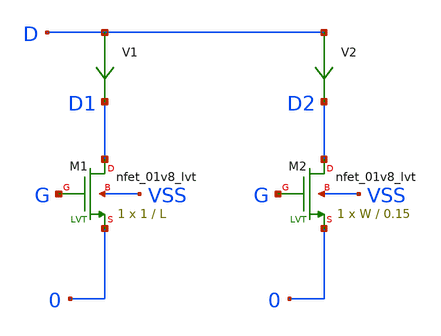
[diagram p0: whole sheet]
** sch_path: sky130_tests/test_nmos_sizes.sch
* Copyright 2021 Stefan Frederik Schippers
* Licensed under the Apache License, Version 2.0 (the "License");
* you may not use this file except in compliance with the License.
* You may obtain a copy of the License at
* https://www.apache.org/licenses/LICENSE-2.0
* Unless required by applicable law or agreed to in writing, software
* distributed under the License is distributed on an "AS IS" BASIS,
* WITHOUT WARRANTIES OR CONDITIONS OF ANY KIND, either express or implied.
* See the License for the specific language governing permissions and
* limitations under the License.
**.subckt test_nmos_sizes
XM1 D1 G 0 VSS sky130_fd_pr__nfet_01v8_lvt L=L W=1 nf=1 ad='W * 0.29' as='W * 0.29' pd='2 * (W + 0.29)'
+ ps='2 * (W + 0.29)' nrd='0.29 / W' nrs='0.29 / W' sa=0 sb=0 sd=0 mult=1 m=1
XM2 D2 G 0 VSS sky130_fd_pr__nfet_01v8_lvt L=0.15 W=W nf=1 ad='W * 0.29' as='W * 0.29' pd='2 * (W + 0.29)'
+ ps='2 * (W + 0.29)' nrd='0.29 / W' nrs='0.29 / W' sa=0 sb=0 sd=0 mult=1 m=1
V2 D D2 0
.save i(v2)
V1 D D1 0
.save i(v1)
**** begin user architecture code
 ** manual skywater pdks install (with patches applied)
* .lib $::SKYWATER_MODELS/models/sky130.lib.spice tt

** opencircuitdesign pdks install
.lib $::SKYWATER_MODELS/sky130.lib.spice tt

.param mc_mm_switch=0
.param mc_pr_switch=0

**** end user architecture code
**.ends
**** begin user architecture code

* .option SCALE=1e-6
.option method=gear seed=12
.param L=0.15
.param W=0.5

vd d 0 0
vg g 0 0
.control
dc vd 0 2 0.01 vg 0 2 0.2
alterparam L=0.18
alterparam W=1
reset
dc vd 0 2 0.01 vg 0 2 0.2
alterparam L=0.3
alterparam W=2
reset
dc vd 0 2 0.01 vg 0 2 0.2
alterparam L=0.5
alterparam W=3
reset
dc vd 0 2 0.01 vg 0 2 0.2

.endc





**** end user architecture code
.end
